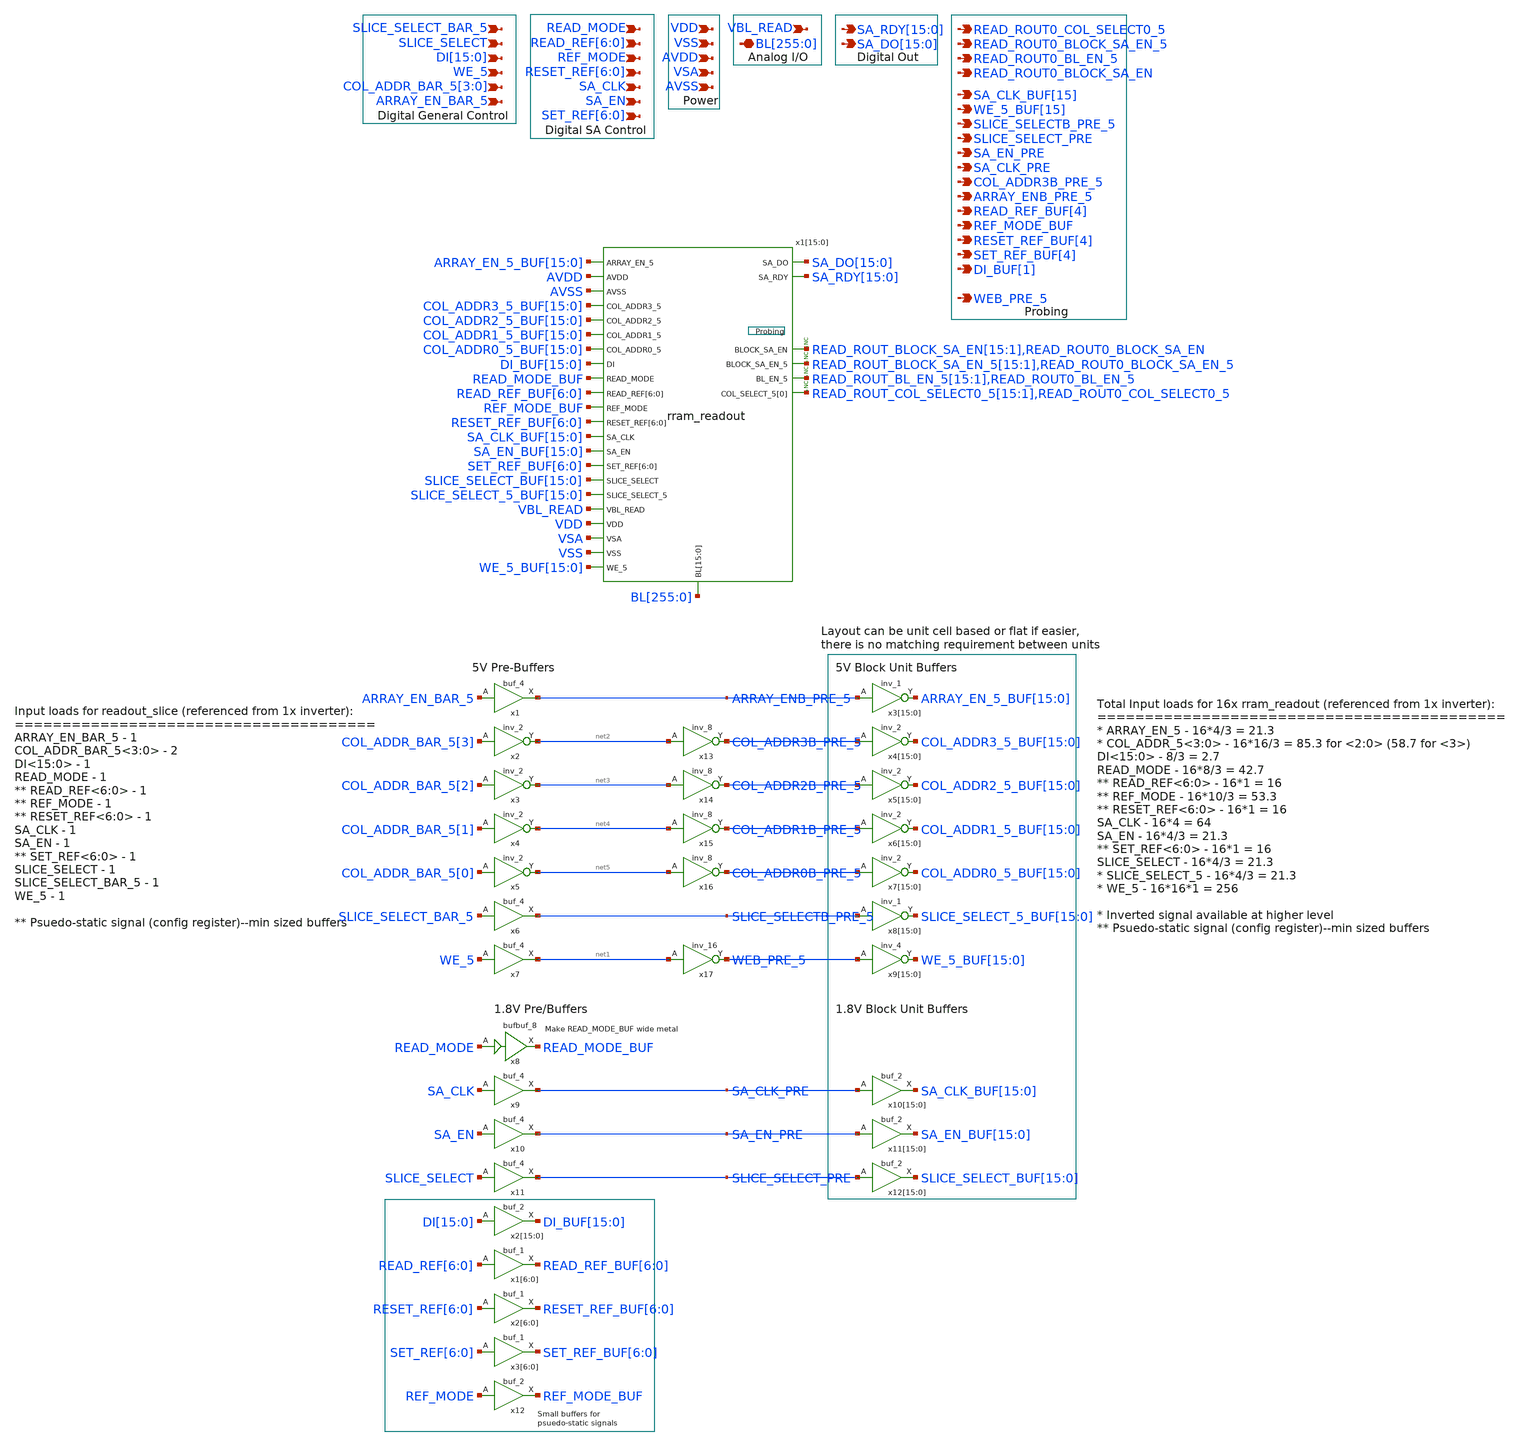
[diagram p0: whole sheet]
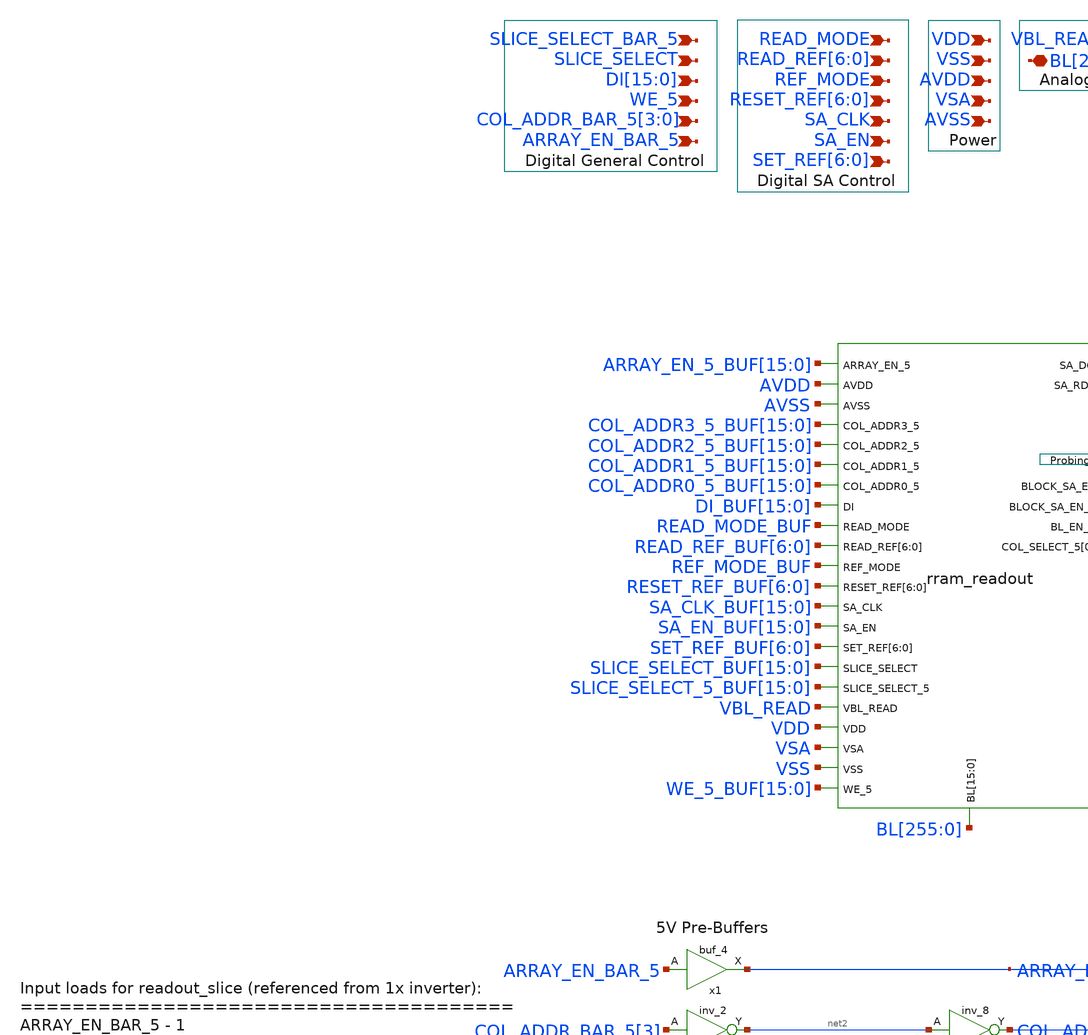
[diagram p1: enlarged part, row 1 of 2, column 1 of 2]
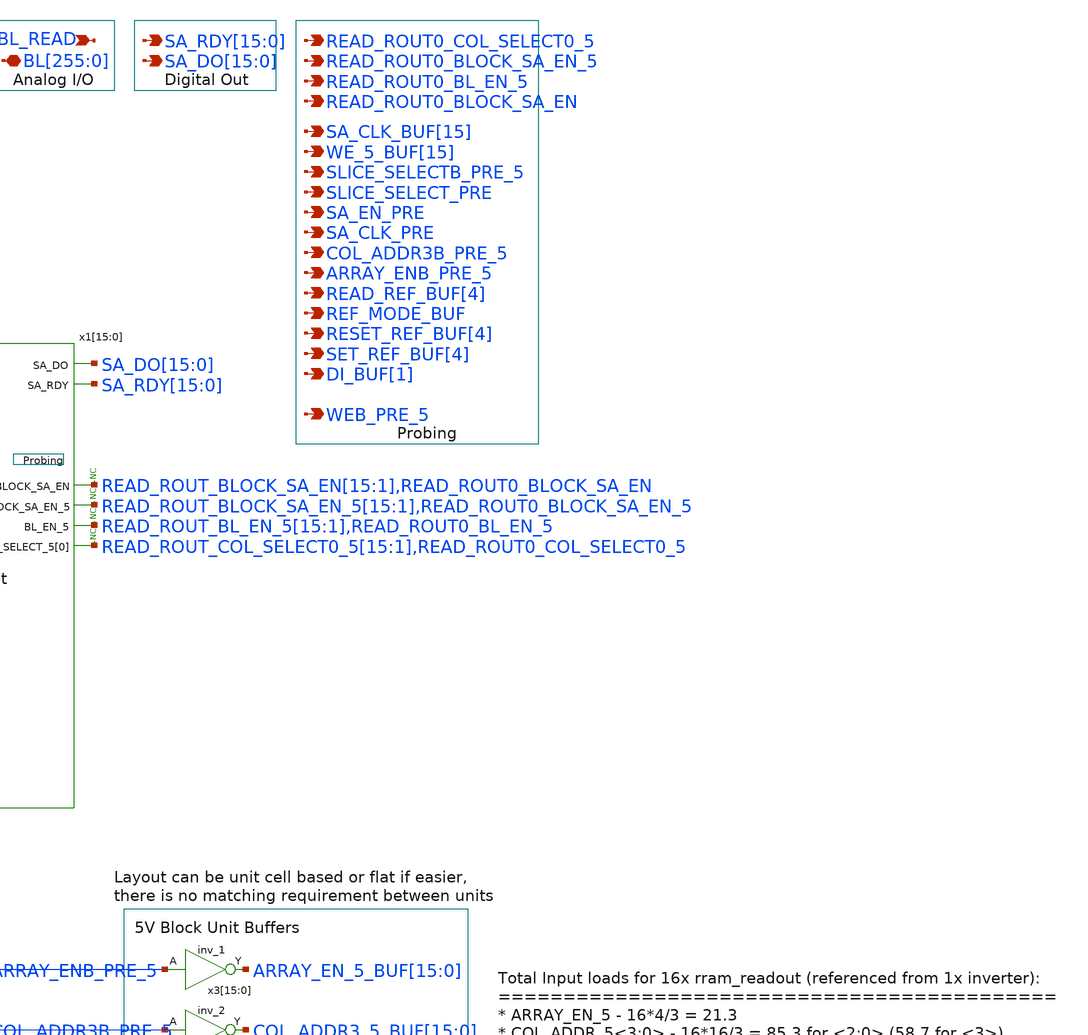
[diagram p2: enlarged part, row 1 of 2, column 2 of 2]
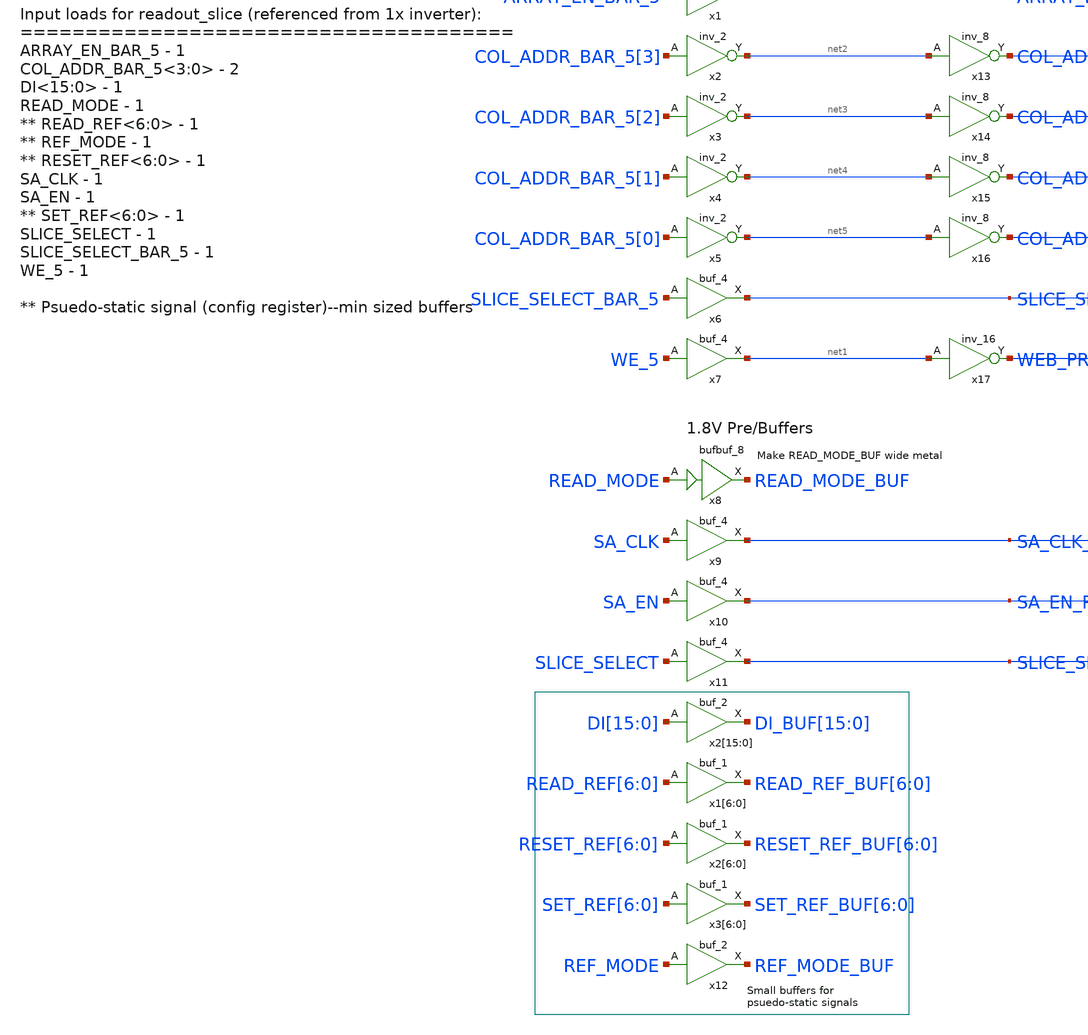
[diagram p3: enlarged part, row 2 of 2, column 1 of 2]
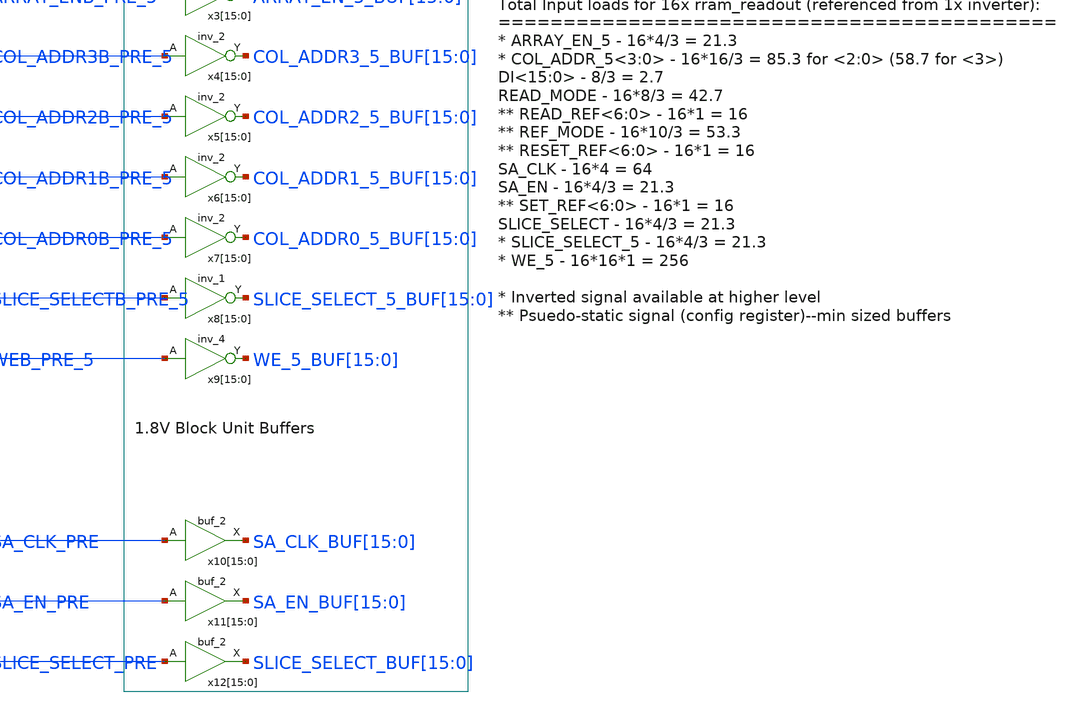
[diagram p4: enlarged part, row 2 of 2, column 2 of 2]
** sch_path: BL_Read_Interface/readout_slice.sch
**.subckt readout_slice SLICE_SELECT_BAR_5 SLICE_SELECT
*+ DI[15],DI[14],DI[13],DI[12],DI[11],DI[10],DI[9],DI[8],DI[7],DI[6],DI[5],DI[4],DI[3],DI[2],DI[1],DI[0] WE_5 COL_ADDR_BAR_5[3],COL_ADDR_BAR_5[2],COL_ADDR_BAR_5[1],COL_ADDR_BAR_5[0] ARRAY_EN_BAR_5 VDD VSS
*+ AVDD VSA AVSS VBL_READ
*+ BL[255],BL[254],BL[253],BL[252],BL[251],BL[250],BL[249],BL[248],BL[247],BL[246],BL[245],BL[244],BL[243],BL[242],BL[241],BL[240],BL[239],BL[238],BL[237],BL[236],BL[235],BL[234],BL[233],BL[232],BL[231],BL[230],BL[229],BL[228],BL[227],BL[226],BL[225],BL[224],BL[223],BL[222],BL[221],BL[220],BL[219],BL[218],BL[217],BL[216],BL[215],BL[214],BL[213],BL[212],BL[211],BL[210],BL[209],BL[208],BL[207],BL[206],BL[205],BL[204],BL[203],BL[202],BL[201],BL[200],BL[199],BL[198],BL[197],BL[196],BL[195],BL[194],BL[193],BL[192],BL[191],BL[190],BL[189],BL[188],BL[187],BL[186],BL[185],BL[184],BL[183],BL[182],BL[181],BL[180],BL[179],BL[178],BL[177],BL[176],BL[175],BL[174],BL[173],BL[172],BL[171],BL[170],BL[169],BL[168],BL[167],BL[166],BL[165],BL[164],BL[163],BL[162],BL[161],BL[160],BL[159],BL[158],BL[157],BL[156],BL[155],BL[154],BL[153],BL[152],BL[151],BL[150],BL[149],BL[148],BL[147],BL[146],BL[145],BL[144],BL[143],BL[142],BL[141],BL[140],BL[139],BL[138],BL[137],BL[136],BL[135],BL[134],BL[133],BL[132],BL[131],BL[130],BL[129],BL[128],BL[127],BL[126],BL[125],BL[124],BL[123],BL[122],BL[121],BL[120],BL[119],BL[118],BL[117],BL[116],BL[115],BL[114],BL[113],BL[112],BL[111],BL[110],BL[109],BL[108],BL[107],BL[106],BL[105],BL[104],BL[103],BL[102],BL[101],BL[100],BL[99],BL[98],BL[97],BL[96],BL[95],BL[94],BL[93],BL[92],BL[91],BL[90],BL[89],BL[88],BL[87],BL[86],BL[85],BL[84],BL[83],BL[82],BL[81],BL[80],BL[79],BL[78],BL[77],BL[76],BL[75],BL[74],BL[73],BL[72],BL[71],BL[70],BL[69],BL[68],BL[67],BL[66],BL[65],BL[64],BL[63],BL[62],BL[61],BL[60],BL[59],BL[58],BL[57],BL[56],BL[55],BL[54],BL[53],BL[52],BL[51],BL[50],BL[49],BL[48],BL[47],BL[46],BL[45],BL[44],BL[43],BL[42],BL[41],BL[40],BL[39],BL[38],BL[37],BL[36],BL[35],BL[34],BL[33],BL[32],BL[31],BL[30],BL[29],BL[28],BL[27],BL[26],BL[25],BL[24],BL[23],BL[22],BL[21],BL[20],BL[19],BL[18],BL[17],BL[16],BL[15],BL[14],BL[13],BL[12],BL[11],BL[10],BL[9],BL[8],BL[7],BL[6],BL[5],BL[4],BL[3],BL[2],BL[1],BL[0]
*+ SA_RDY[15],SA_RDY[14],SA_RDY[13],SA_RDY[12],SA_RDY[11],SA_RDY[10],SA_RDY[9],SA_RDY[8],SA_RDY[7],SA_RDY[6],SA_RDY[5],SA_RDY[4],SA_RDY[3],SA_RDY[2],SA_RDY[1],SA_RDY[0]
*+ SA_DO[15],SA_DO[14],SA_DO[13],SA_DO[12],SA_DO[11],SA_DO[10],SA_DO[9],SA_DO[8],SA_DO[7],SA_DO[6],SA_DO[5],SA_DO[4],SA_DO[3],SA_DO[2],SA_DO[1],SA_DO[0] READ_MODE READ_REF[6],READ_REF[5],READ_REF[4],READ_REF[3],READ_REF[2],READ_REF[1],READ_REF[0]
*+ REF_MODE RESET_REF[6],RESET_REF[5],RESET_REF[4],RESET_REF[3],RESET_REF[2],RESET_REF[1],RESET_REF[0] SA_CLK
*+ SA_EN SET_REF[6],SET_REF[5],SET_REF[4],SET_REF[3],SET_REF[2],SET_REF[1],SET_REF[0]
*+ READ_ROUT0_COL_SELECT0_5 READ_ROUT0_BLOCK_SA_EN_5 READ_ROUT0_BL_EN_5 READ_ROUT0_BLOCK_SA_EN SA_CLK_BUF[15] WE_5_BUF[15]
*+ SLICE_SELECTB_PRE_5 SLICE_SELECT_PRE SA_EN_PRE SA_CLK_PRE COL_ADDR3B_PRE_5 ARRAY_ENB_PRE_5 READ_REF_BUF[4] REF_MODE_BUF
*+ RESET_REF_BUF[4] SET_REF_BUF[4] DI_BUF[1] WEB_PRE_5
*.ipin SLICE_SELECT_BAR_5
*.ipin SLICE_SELECT
*.ipin
*+ DI[15],DI[14],DI[13],DI[12],DI[11],DI[10],DI[9],DI[8],DI[7],DI[6],DI[5],DI[4],DI[3],DI[2],DI[1],DI[0]
*.ipin WE_5
*.ipin COL_ADDR_BAR_5[3],COL_ADDR_BAR_5[2],COL_ADDR_BAR_5[1],COL_ADDR_BAR_5[0]
*.ipin ARRAY_EN_BAR_5
*.ipin VDD
*.ipin VSS
*.ipin AVDD
*.ipin VSA
*.ipin AVSS
*.ipin VBL_READ
*.iopin
*+ BL[255],BL[254],BL[253],BL[252],BL[251],BL[250],BL[249],BL[248],BL[247],BL[246],BL[245],BL[244],BL[243],BL[242],BL[241],BL[240],BL[239],BL[238],BL[237],BL[236],BL[235],BL[234],BL[233],BL[232],BL[231],BL[230],BL[229],BL[228],BL[227],BL[226],BL[225],BL[224],BL[223],BL[222],BL[221],BL[220],BL[219],BL[218],BL[217],BL[216],BL[215],BL[214],BL[213],BL[212],BL[211],BL[210],BL[209],BL[208],BL[207],BL[206],BL[205],BL[204],BL[203],BL[202],BL[201],BL[200],BL[199],BL[198],BL[197],BL[196],BL[195],BL[194],BL[193],BL[192],BL[191],BL[190],BL[189],BL[188],BL[187],BL[186],BL[185],BL[184],BL[183],BL[182],BL[181],BL[180],BL[179],BL[178],BL[177],BL[176],BL[175],BL[174],BL[173],BL[172],BL[171],BL[170],BL[169],BL[168],BL[167],BL[166],BL[165],BL[164],BL[163],BL[162],BL[161],BL[160],BL[159],BL[158],BL[157],BL[156],BL[155],BL[154],BL[153],BL[152],BL[151],BL[150],BL[149],BL[148],BL[147],BL[146],BL[145],BL[144],BL[143],BL[142],BL[141],BL[140],BL[139],BL[138],BL[137],BL[136],BL[135],BL[134],BL[133],BL[132],BL[131],BL[130],BL[129],BL[128],BL[127],BL[126],BL[125],BL[124],BL[123],BL[122],BL[121],BL[120],BL[119],BL[118],BL[117],BL[116],BL[115],BL[114],BL[113],BL[112],BL[111],BL[110],BL[109],BL[108],BL[107],BL[106],BL[105],BL[104],BL[103],BL[102],BL[101],BL[100],BL[99],BL[98],BL[97],BL[96],BL[95],BL[94],BL[93],BL[92],BL[91],BL[90],BL[89],BL[88],BL[87],BL[86],BL[85],BL[84],BL[83],BL[82],BL[81],BL[80],BL[79],BL[78],BL[77],BL[76],BL[75],BL[74],BL[73],BL[72],BL[71],BL[70],BL[69],BL[68],BL[67],BL[66],BL[65],BL[64],BL[63],BL[62],BL[61],BL[60],BL[59],BL[58],BL[57],BL[56],BL[55],BL[54],BL[53],BL[52],BL[51],BL[50],BL[49],BL[48],BL[47],BL[46],BL[45],BL[44],BL[43],BL[42],BL[41],BL[40],BL[39],BL[38],BL[37],BL[36],BL[35],BL[34],BL[33],BL[32],BL[31],BL[30],BL[29],BL[28],BL[27],BL[26],BL[25],BL[24],BL[23],BL[22],BL[21],BL[20],BL[19],BL[18],BL[17],BL[16],BL[15],BL[14],BL[13],BL[12],BL[11],BL[10],BL[9],BL[8],BL[7],BL[6],BL[5],BL[4],BL[3],BL[2],BL[1],BL[0]
*.opin
*+ SA_RDY[15],SA_RDY[14],SA_RDY[13],SA_RDY[12],SA_RDY[11],SA_RDY[10],SA_RDY[9],SA_RDY[8],SA_RDY[7],SA_RDY[6],SA_RDY[5],SA_RDY[4],SA_RDY[3],SA_RDY[2],SA_RDY[1],SA_RDY[0]
*.opin
*+ SA_DO[15],SA_DO[14],SA_DO[13],SA_DO[12],SA_DO[11],SA_DO[10],SA_DO[9],SA_DO[8],SA_DO[7],SA_DO[6],SA_DO[5],SA_DO[4],SA_DO[3],SA_DO[2],SA_DO[1],SA_DO[0]
*.ipin READ_MODE
*.ipin READ_REF[6],READ_REF[5],READ_REF[4],READ_REF[3],READ_REF[2],READ_REF[1],READ_REF[0]
*.ipin REF_MODE
*.ipin RESET_REF[6],RESET_REF[5],RESET_REF[4],RESET_REF[3],RESET_REF[2],RESET_REF[1],RESET_REF[0]
*.ipin SA_CLK
*.ipin SA_EN
*.ipin SET_REF[6],SET_REF[5],SET_REF[4],SET_REF[3],SET_REF[2],SET_REF[1],SET_REF[0]
*.opin READ_ROUT0_COL_SELECT0_5
*.opin READ_ROUT0_BLOCK_SA_EN_5
*.opin READ_ROUT0_BL_EN_5
*.opin READ_ROUT0_BLOCK_SA_EN
*.opin SA_CLK_BUF[15]
*.opin WE_5_BUF[15]
*.opin SLICE_SELECTB_PRE_5
*.opin SLICE_SELECT_PRE
*.opin SA_EN_PRE
*.opin SA_CLK_PRE
*.opin COL_ADDR3B_PRE_5
*.opin ARRAY_ENB_PRE_5
*.opin READ_REF_BUF[4]
*.opin REF_MODE_BUF
*.opin RESET_REF_BUF[4]
*.opin SET_REF_BUF[4]
*.opin DI_BUF[1]
*.opin WEB_PRE_5
x1[15] VDD SLICE_SELECT_BUF[15] READ_ROUT_COL_SELECT0_5[15] VBL_READ READ_MODE_BUF BL[255] BL[254]
+ BL[253] BL[252] BL[251] BL[250] BL[249] BL[248] BL[247] BL[246] BL[245] BL[244] BL[243] BL[242] BL[241]
+ BL[240] READ_ROUT_BLOCK_SA_EN[15] DI_BUF[15] READ_REF_BUF[6] READ_REF_BUF[5] READ_REF_BUF[4]
+ READ_REF_BUF[3] READ_REF_BUF[2] READ_REF_BUF[1] READ_REF_BUF[0] VSS READ_ROUT_BLOCK_SA_EN_5[15] AVDD REF_MODE_BUF
+ SLICE_SELECT_5_BUF[15] READ_ROUT_BL_EN_5[15] WE_5_BUF[15] VSA RESET_REF_BUF[6] RESET_REF_BUF[5] RESET_REF_BUF[4]
+ RESET_REF_BUF[3] RESET_REF_BUF[2] RESET_REF_BUF[1] RESET_REF_BUF[0] AVSS COL_ADDR3_5_BUF[15] SET_REF_BUF[6]
+ SET_REF_BUF[5] SET_REF_BUF[4] SET_REF_BUF[3] SET_REF_BUF[2] SET_REF_BUF[1] SET_REF_BUF[0] COL_ADDR2_5_BUF[15]
+ SA_EN_BUF[15] COL_ADDR1_5_BUF[15] SA_CLK_BUF[15] SA_DO[15] COL_ADDR0_5_BUF[15] SA_RDY[15] ARRAY_EN_5_BUF[15]
+ rram_readout
x1[14] VDD SLICE_SELECT_BUF[14] READ_ROUT_COL_SELECT0_5[14] VBL_READ READ_MODE_BUF BL[239] BL[238]
+ BL[237] BL[236] BL[235] BL[234] BL[233] BL[232] BL[231] BL[230] BL[229] BL[228] BL[227] BL[226] BL[225]
+ BL[224] READ_ROUT_BLOCK_SA_EN[14] DI_BUF[14] READ_REF_BUF[6] READ_REF_BUF[5] READ_REF_BUF[4]
+ READ_REF_BUF[3] READ_REF_BUF[2] READ_REF_BUF[1] READ_REF_BUF[0] VSS READ_ROUT_BLOCK_SA_EN_5[14] AVDD REF_MODE_BUF
+ SLICE_SELECT_5_BUF[14] READ_ROUT_BL_EN_5[14] WE_5_BUF[14] VSA RESET_REF_BUF[6] RESET_REF_BUF[5] RESET_REF_BUF[4]
+ RESET_REF_BUF[3] RESET_REF_BUF[2] RESET_REF_BUF[1] RESET_REF_BUF[0] AVSS COL_ADDR3_5_BUF[14] SET_REF_BUF[6]
+ SET_REF_BUF[5] SET_REF_BUF[4] SET_REF_BUF[3] SET_REF_BUF[2] SET_REF_BUF[1] SET_REF_BUF[0] COL_ADDR2_5_BUF[14]
+ SA_EN_BUF[14] COL_ADDR1_5_BUF[14] SA_CLK_BUF[14] SA_DO[14] COL_ADDR0_5_BUF[14] SA_RDY[14] ARRAY_EN_5_BUF[14]
+ rram_readout
x1[13] VDD SLICE_SELECT_BUF[13] READ_ROUT_COL_SELECT0_5[13] VBL_READ READ_MODE_BUF BL[223] BL[222]
+ BL[221] BL[220] BL[219] BL[218] BL[217] BL[216] BL[215] BL[214] BL[213] BL[212] BL[211] BL[210] BL[209]
+ BL[208] READ_ROUT_BLOCK_SA_EN[13] DI_BUF[13] READ_REF_BUF[6] READ_REF_BUF[5] READ_REF_BUF[4]
+ READ_REF_BUF[3] READ_REF_BUF[2] READ_REF_BUF[1] READ_REF_BUF[0] VSS READ_ROUT_BLOCK_SA_EN_5[13] AVDD REF_MODE_BUF
+ SLICE_SELECT_5_BUF[13] READ_ROUT_BL_EN_5[13] WE_5_BUF[13] VSA RESET_REF_BUF[6] RESET_REF_BUF[5] RESET_REF_BUF[4]
+ RESET_REF_BUF[3] RESET_REF_BUF[2] RESET_REF_BUF[1] RESET_REF_BUF[0] AVSS COL_ADDR3_5_BUF[13] SET_REF_BUF[6]
+ SET_REF_BUF[5] SET_REF_BUF[4] SET_REF_BUF[3] SET_REF_BUF[2] SET_REF_BUF[1] SET_REF_BUF[0] COL_ADDR2_5_BUF[13]
+ SA_EN_BUF[13] COL_ADDR1_5_BUF[13] SA_CLK_BUF[13] SA_DO[13] COL_ADDR0_5_BUF[13] SA_RDY[13] ARRAY_EN_5_BUF[13]
+ rram_readout
x1[12] VDD SLICE_SELECT_BUF[12] READ_ROUT_COL_SELECT0_5[12] VBL_READ READ_MODE_BUF BL[207] BL[206]
+ BL[205] BL[204] BL[203] BL[202] BL[201] BL[200] BL[199] BL[198] BL[197] BL[196] BL[195] BL[194] BL[193]
+ BL[192] READ_ROUT_BLOCK_SA_EN[12] DI_BUF[12] READ_REF_BUF[6] READ_REF_BUF[5] READ_REF_BUF[4]
+ READ_REF_BUF[3] READ_REF_BUF[2] READ_REF_BUF[1] READ_REF_BUF[0] VSS READ_ROUT_BLOCK_SA_EN_5[12] AVDD REF_MODE_BUF
+ SLICE_SELECT_5_BUF[12] READ_ROUT_BL_EN_5[12] WE_5_BUF[12] VSA RESET_REF_BUF[6] RESET_REF_BUF[5] RESET_REF_BUF[4]
+ RESET_REF_BUF[3] RESET_REF_BUF[2] RESET_REF_BUF[1] RESET_REF_BUF[0] AVSS COL_ADDR3_5_BUF[12] SET_REF_BUF[6]
+ SET_REF_BUF[5] SET_REF_BUF[4] SET_REF_BUF[3] SET_REF_BUF[2] SET_REF_BUF[1] SET_REF_BUF[0] COL_ADDR2_5_BUF[12]
+ SA_EN_BUF[12] COL_ADDR1_5_BUF[12] SA_CLK_BUF[12] SA_DO[12] COL_ADDR0_5_BUF[12] SA_RDY[12] ARRAY_EN_5_BUF[12]
+ rram_readout
x1[11] VDD SLICE_SELECT_BUF[11] READ_ROUT_COL_SELECT0_5[11] VBL_READ READ_MODE_BUF BL[191] BL[190]
+ BL[189] BL[188] BL[187] BL[186] BL[185] BL[184] BL[183] BL[182] BL[181] BL[180] BL[179] BL[178] BL[177]
+ BL[176] READ_ROUT_BLOCK_SA_EN[11] DI_BUF[11] READ_REF_BUF[6] READ_REF_BUF[5] READ_REF_BUF[4]
+ READ_REF_BUF[3] READ_REF_BUF[2] READ_REF_BUF[1] READ_REF_BUF[0] VSS READ_ROUT_BLOCK_SA_EN_5[11] AVDD REF_MODE_BUF
+ SLICE_SELECT_5_BUF[11] READ_ROUT_BL_EN_5[11] WE_5_BUF[11] VSA RESET_REF_BUF[6] RESET_REF_BUF[5] RESET_REF_BUF[4]
+ RESET_REF_BUF[3] RESET_REF_BUF[2] RESET_REF_BUF[1] RESET_REF_BUF[0] AVSS COL_ADDR3_5_BUF[11] SET_REF_BUF[6]
+ SET_REF_BUF[5] SET_REF_BUF[4] SET_REF_BUF[3] SET_REF_BUF[2] SET_REF_BUF[1] SET_REF_BUF[0] COL_ADDR2_5_BUF[11]
+ SA_EN_BUF[11] COL_ADDR1_5_BUF[11] SA_CLK_BUF[11] SA_DO[11] COL_ADDR0_5_BUF[11] SA_RDY[11] ARRAY_EN_5_BUF[11]
+ rram_readout
x1[10] VDD SLICE_SELECT_BUF[10] READ_ROUT_COL_SELECT0_5[10] VBL_READ READ_MODE_BUF BL[175] BL[174]
+ BL[173] BL[172] BL[171] BL[170] BL[169] BL[168] BL[167] BL[166] BL[165] BL[164] BL[163] BL[162] BL[161]
+ BL[160] READ_ROUT_BLOCK_SA_EN[10] DI_BUF[10] READ_REF_BUF[6] READ_REF_BUF[5] READ_REF_BUF[4]
+ READ_REF_BUF[3] READ_REF_BUF[2] READ_REF_BUF[1] READ_REF_BUF[0] VSS READ_ROUT_BLOCK_SA_EN_5[10] AVDD REF_MODE_BUF
+ SLICE_SELECT_5_BUF[10] READ_ROUT_BL_EN_5[10] WE_5_BUF[10] VSA RESET_REF_BUF[6] RESET_REF_BUF[5] RESET_REF_BUF[4]
+ RESET_REF_BUF[3] RESET_REF_BUF[2] RESET_REF_BUF[1] RESET_REF_BUF[0] AVSS COL_ADDR3_5_BUF[10] SET_REF_BUF[6]
+ SET_REF_BUF[5] SET_REF_BUF[4] SET_REF_BUF[3] SET_REF_BUF[2] SET_REF_BUF[1] SET_REF_BUF[0] COL_ADDR2_5_BUF[10]
+ SA_EN_BUF[10] COL_ADDR1_5_BUF[10] SA_CLK_BUF[10] SA_DO[10] COL_ADDR0_5_BUF[10] SA_RDY[10] ARRAY_EN_5_BUF[10]
+ rram_readout
x1[9] VDD SLICE_SELECT_BUF[9] READ_ROUT_COL_SELECT0_5[9] VBL_READ READ_MODE_BUF BL[159] BL[158]
+ BL[157] BL[156] BL[155] BL[154] BL[153] BL[152] BL[151] BL[150] BL[149] BL[148] BL[147] BL[146] BL[145]
+ BL[144] READ_ROUT_BLOCK_SA_EN[9] DI_BUF[9] READ_REF_BUF[6] READ_REF_BUF[5] READ_REF_BUF[4] READ_REF_BUF[3]
+ READ_REF_BUF[2] READ_REF_BUF[1] READ_REF_BUF[0] VSS READ_ROUT_BLOCK_SA_EN_5[9] AVDD REF_MODE_BUF
+ SLICE_SELECT_5_BUF[9] READ_ROUT_BL_EN_5[9] WE_5_BUF[9] VSA RESET_REF_BUF[6] RESET_REF_BUF[5] RESET_REF_BUF[4]
+ RESET_REF_BUF[3] RESET_REF_BUF[2] RESET_REF_BUF[1] RESET_REF_BUF[0] AVSS COL_ADDR3_5_BUF[9] SET_REF_BUF[6]
+ SET_REF_BUF[5] SET_REF_BUF[4] SET_REF_BUF[3] SET_REF_BUF[2] SET_REF_BUF[1] SET_REF_BUF[0] COL_ADDR2_5_BUF[9]
+ SA_EN_BUF[9] COL_ADDR1_5_BUF[9] SA_CLK_BUF[9] SA_DO[9] COL_ADDR0_5_BUF[9] SA_RDY[9] ARRAY_EN_5_BUF[9]
+ rram_readout
x1[8] VDD SLICE_SELECT_BUF[8] READ_ROUT_COL_SELECT0_5[8] VBL_READ READ_MODE_BUF BL[143] BL[142]
+ BL[141] BL[140] BL[139] BL[138] BL[137] BL[136] BL[135] BL[134] BL[133] BL[132] BL[131] BL[130] BL[129]
+ BL[128] READ_ROUT_BLOCK_SA_EN[8] DI_BUF[8] READ_REF_BUF[6] READ_REF_BUF[5] READ_REF_BUF[4] READ_REF_BUF[3]
+ READ_REF_BUF[2] READ_REF_BUF[1] READ_REF_BUF[0] VSS READ_ROUT_BLOCK_SA_EN_5[8] AVDD REF_MODE_BUF
+ SLICE_SELECT_5_BUF[8] READ_ROUT_BL_EN_5[8] WE_5_BUF[8] VSA RESET_REF_BUF[6] RESET_REF_BUF[5] RESET_REF_BUF[4]
+ RESET_REF_BUF[3] RESET_REF_BUF[2] RESET_REF_BUF[1] RESET_REF_BUF[0] AVSS COL_ADDR3_5_BUF[8] SET_REF_BUF[6]
+ SET_REF_BUF[5] SET_REF_BUF[4] SET_REF_BUF[3] SET_REF_BUF[2] SET_REF_BUF[1] SET_REF_BUF[0] COL_ADDR2_5_BUF[8]
+ SA_EN_BUF[8] COL_ADDR1_5_BUF[8] SA_CLK_BUF[8] SA_DO[8] COL_ADDR0_5_BUF[8] SA_RDY[8] ARRAY_EN_5_BUF[8]
+ rram_readout
x1[7] VDD SLICE_SELECT_BUF[7] READ_ROUT_COL_SELECT0_5[7] VBL_READ READ_MODE_BUF BL[127] BL[126]
+ BL[125] BL[124] BL[123] BL[122] BL[121] BL[120] BL[119] BL[118] BL[117] BL[116] BL[115] BL[114] BL[113]
+ BL[112] READ_ROUT_BLOCK_SA_EN[7] DI_BUF[7] READ_REF_BUF[6] READ_REF_BUF[5] READ_REF_BUF[4] READ_REF_BUF[3]
+ READ_REF_BUF[2] READ_REF_BUF[1] READ_REF_BUF[0] VSS READ_ROUT_BLOCK_SA_EN_5[7] AVDD REF_MODE_BUF
+ SLICE_SELECT_5_BUF[7] READ_ROUT_BL_EN_5[7] WE_5_BUF[7] VSA RESET_REF_BUF[6] RESET_REF_BUF[5] RESET_REF_BUF[4]
+ RESET_REF_BUF[3] RESET_REF_BUF[2] RESET_REF_BUF[1] RESET_REF_BUF[0] AVSS COL_ADDR3_5_BUF[7] SET_REF_BUF[6]
+ SET_REF_BUF[5] SET_REF_BUF[4] SET_REF_BUF[3] SET_REF_BUF[2] SET_REF_BUF[1] SET_REF_BUF[0] COL_ADDR2_5_BUF[7]
+ SA_EN_BUF[7] COL_ADDR1_5_BUF[7] SA_CLK_BUF[7] SA_DO[7] COL_ADDR0_5_BUF[7] SA_RDY[7] ARRAY_EN_5_BUF[7]
+ rram_readout
x1[6] VDD SLICE_SELECT_BUF[6] READ_ROUT_COL_SELECT0_5[6] VBL_READ READ_MODE_BUF BL[111] BL[110]
+ BL[109] BL[108] BL[107] BL[106] BL[105] BL[104] BL[103] BL[102] BL[101] BL[100] BL[99] BL[98] BL[97] BL[96]
+ READ_ROUT_BLOCK_SA_EN[6] DI_BUF[6] READ_REF_BUF[6] READ_REF_BUF[5] READ_REF_BUF[4] READ_REF_BUF[3] READ_REF_BUF[2]
+ READ_REF_BUF[1] READ_REF_BUF[0] VSS READ_ROUT_BLOCK_SA_EN_5[6] AVDD REF_MODE_BUF SLICE_SELECT_5_BUF[6]
+ READ_ROUT_BL_EN_5[6] WE_5_BUF[6] VSA RESET_REF_BUF[6] RESET_REF_BUF[5] RESET_REF_BUF[4] RESET_REF_BUF[3]
+ RESET_REF_BUF[2] RESET_REF_BUF[1] RESET_REF_BUF[0] AVSS COL_ADDR3_5_BUF[6] SET_REF_BUF[6] SET_REF_BUF[5]
+ SET_REF_BUF[4] SET_REF_BUF[3] SET_REF_BUF[2] SET_REF_BUF[1] SET_REF_BUF[0] COL_ADDR2_5_BUF[6] SA_EN_BUF[6]
+ COL_ADDR1_5_BUF[6] SA_CLK_BUF[6] SA_DO[6] COL_ADDR0_5_BUF[6] SA_RDY[6] ARRAY_EN_5_BUF[6] rram_readout
x1[5] VDD SLICE_SELECT_BUF[5] READ_ROUT_COL_SELECT0_5[5] VBL_READ READ_MODE_BUF BL[95] BL[94] BL[93]
+ BL[92] BL[91] BL[90] BL[89] BL[88] BL[87] BL[86] BL[85] BL[84] BL[83] BL[82] BL[81] BL[80]
+ READ_ROUT_BLOCK_SA_EN[5] DI_BUF[5] READ_REF_BUF[6] READ_REF_BUF[5] READ_REF_BUF[4] READ_REF_BUF[3] READ_REF_BUF[2]
+ READ_REF_BUF[1] READ_REF_BUF[0] VSS READ_ROUT_BLOCK_SA_EN_5[5] AVDD REF_MODE_BUF SLICE_SELECT_5_BUF[5]
+ READ_ROUT_BL_EN_5[5] WE_5_BUF[5] VSA RESET_REF_BUF[6] RESET_REF_BUF[5] RESET_REF_BUF[4] RESET_REF_BUF[3]
+ RESET_REF_BUF[2] RESET_REF_BUF[1] RESET_REF_BUF[0] AVSS COL_ADDR3_5_BUF[5] SET_REF_BUF[6] SET_REF_BUF[5]
+ SET_REF_BUF[4] SET_REF_BUF[3] SET_REF_BUF[2] SET_REF_BUF[1] SET_REF_BUF[0] COL_ADDR2_5_BUF[5] SA_EN_BUF[5]
+ COL_ADDR1_5_BUF[5] SA_CLK_BUF[5] SA_DO[5] COL_ADDR0_5_BUF[5] SA_RDY[5] ARRAY_EN_5_BUF[5] rram_readout
x1[4] VDD SLICE_SELECT_BUF[4] READ_ROUT_COL_SELECT0_5[4] VBL_READ READ_MODE_BUF BL[79] BL[78] BL[77]
+ BL[76] BL[75] BL[74] BL[73] BL[72] BL[71] BL[70] BL[69] BL[68] BL[67] BL[66] BL[65] BL[64]
+ READ_ROUT_BLOCK_SA_EN[4] DI_BUF[4] READ_REF_BUF[6] READ_REF_BUF[5] READ_REF_BUF[4] READ_REF_BUF[3] READ_REF_BUF[2]
+ READ_REF_BUF[1] READ_REF_BUF[0] VSS READ_ROUT_BLOCK_SA_EN_5[4] AVDD REF_MODE_BUF SLICE_SELECT_5_BUF[4]
+ READ_ROUT_BL_EN_5[4] WE_5_BUF[4] VSA RESET_REF_BUF[6] RESET_REF_BUF[5] RESET_REF_BUF[4] RESET_REF_BUF[3]
+ RESET_REF_BUF[2] RESET_REF_BUF[1] RESET_REF_BUF[0] AVSS COL_ADDR3_5_BUF[4] SET_REF_BUF[6] SET_REF_BUF[5]
+ SET_REF_BUF[4] SET_REF_BUF[3] SET_REF_BUF[2] SET_REF_BUF[1] SET_REF_BUF[0] COL_ADDR2_5_BUF[4] SA_EN_BUF[4]
+ COL_ADDR1_5_BUF[4] SA_CLK_BUF[4] SA_DO[4] COL_ADDR0_5_BUF[4] SA_RDY[4] ARRAY_EN_5_BUF[4] rram_readout
x1[3] VDD SLICE_SELECT_BUF[3] READ_ROUT_COL_SELECT0_5[3] VBL_READ READ_MODE_BUF BL[63] BL[62] BL[61]
+ BL[60] BL[59] BL[58] BL[57] BL[56] BL[55] BL[54] BL[53] BL[52] BL[51] BL[50] BL[49] BL[48]
+ READ_ROUT_BLOCK_SA_EN[3] DI_BUF[3] READ_REF_BUF[6] READ_REF_BUF[5] READ_REF_BUF[4] READ_REF_BUF[3] READ_REF_BUF[2]
+ READ_REF_BUF[1] READ_REF_BUF[0] VSS READ_ROUT_BLOCK_SA_EN_5[3] AVDD REF_MODE_BUF SLICE_SELECT_5_BUF[3]
+ READ_ROUT_BL_EN_5[3] WE_5_BUF[3] VSA RESET_REF_BUF[6] RESET_REF_BUF[5] RESET_REF_BUF[4] RESET_REF_BUF[3]
+ RESET_REF_BUF[2] RESET_REF_BUF[1] RESET_REF_BUF[0] AVSS COL_ADDR3_5_BUF[3] SET_REF_BUF[6] SET_REF_BUF[5]
+ SET_REF_BUF[4] SET_REF_BUF[3] SET_REF_BUF[2] SET_REF_BUF[1] SET_REF_BUF[0] COL_ADDR2_5_BUF[3] SA_EN_BUF[3]
+ COL_ADDR1_5_BUF[3] SA_CLK_BUF[3] SA_DO[3] COL_ADDR0_5_BUF[3] SA_RDY[3] ARRAY_EN_5_BUF[3] rram_readout
x1[2] VDD SLICE_SELECT_BUF[2] READ_ROUT_COL_SELECT0_5[2] VBL_READ READ_MODE_BUF BL[47] BL[46] BL[45]
+ BL[44] BL[43] BL[42] BL[41] BL[40] BL[39] BL[38] BL[37] BL[36] BL[35] BL[34] BL[33] BL[32]
+ READ_ROUT_BLOCK_SA_EN[2] DI_BUF[2] READ_REF_BUF[6] READ_REF_BUF[5] READ_REF_BUF[4] READ_REF_BUF[3] READ_REF_BUF[2]
+ READ_REF_BUF[1] READ_REF_BUF[0] VSS READ_ROUT_BLOCK_SA_EN_5[2] AVDD REF_MODE_BUF SLICE_SELECT_5_BUF[2]
+ READ_ROUT_BL_EN_5[2] WE_5_BUF[2] VSA RESET_REF_BUF[6] RESET_REF_BUF[5] RESET_REF_BUF[4] RESET_REF_BUF[3]
+ RESET_REF_BUF[2] RESET_REF_BUF[1] RESET_REF_BUF[0] AVSS COL_ADDR3_5_BUF[2] SET_REF_BUF[6] SET_REF_BUF[5]
+ SET_REF_BUF[4] SET_REF_BUF[3] SET_REF_BUF[2] SET_REF_BUF[1] SET_REF_BUF[0] COL_ADDR2_5_BUF[2] SA_EN_BUF[2]
+ COL_ADDR1_5_BUF[2] SA_CLK_BUF[2] SA_DO[2] COL_ADDR0_5_BUF[2] SA_RDY[2] ARRAY_EN_5_BUF[2] rram_readout
x1[1] VDD SLICE_SELECT_BUF[1] READ_ROUT_COL_SELECT0_5[1] VBL_READ READ_MODE_BUF BL[31] BL[30] BL[29]
+ BL[28] BL[27] BL[26] BL[25] BL[24] BL[23] BL[22] BL[21] BL[20] BL[19] BL[18] BL[17] BL[16]
+ READ_ROUT_BLOCK_SA_EN[1] DI_BUF[1] READ_REF_BUF[6] READ_REF_BUF[5] READ_REF_BUF[4] READ_REF_BUF[3] READ_REF_BUF[2]
+ READ_REF_BUF[1] READ_REF_BUF[0] VSS READ_ROUT_BLOCK_SA_EN_5[1] AVDD REF_MODE_BUF SLICE_SELECT_5_BUF[1]
+ READ_ROUT_BL_EN_5[1] WE_5_BUF[1] VSA RESET_REF_BUF[6] RESET_REF_BUF[5] RESET_REF_BUF[4] RESET_REF_BUF[3]
+ RESET_REF_BUF[2] RESET_REF_BUF[1] RESET_REF_BUF[0] AVSS COL_ADDR3_5_BUF[1] SET_REF_BUF[6] SET_REF_BUF[5]
+ SET_REF_BUF[4] SET_REF_BUF[3] SET_REF_BUF[2] SET_REF_BUF[1] SET_REF_BUF[0] COL_ADDR2_5_BUF[1] SA_EN_BUF[1]
+ COL_ADDR1_5_BUF[1] SA_CLK_BUF[1] SA_DO[1] COL_ADDR0_5_BUF[1] SA_RDY[1] ARRAY_EN_5_BUF[1] rram_readout
x1[0] VDD SLICE_SELECT_BUF[0] READ_ROUT0_COL_SELECT0_5 VBL_READ READ_MODE_BUF BL[15] BL[14] BL[13]
+ BL[12] BL[11] BL[10] BL[9] BL[8] BL[7] BL[6] BL[5] BL[4] BL[3] BL[2] BL[1] BL[0] READ_ROUT0_BLOCK_SA_EN
+ DI_BUF[0] READ_REF_BUF[6] READ_REF_BUF[5] READ_REF_BUF[4] READ_REF_BUF[3] READ_REF_BUF[2] READ_REF_BUF[1]
+ READ_REF_BUF[0] VSS READ_ROUT0_BLOCK_SA_EN_5 AVDD REF_MODE_BUF SLICE_SELECT_5_BUF[0] READ_ROUT0_BL_EN_5 WE_5_BUF[0]
+ VSA RESET_REF_BUF[6] RESET_REF_BUF[5] RESET_REF_BUF[4] RESET_REF_BUF[3] RESET_REF_BUF[2]
+ RESET_REF_BUF[1] RESET_REF_BUF[0] AVSS COL_ADDR3_5_BUF[0] SET_REF_BUF[6] SET_REF_BUF[5] SET_REF_BUF[4]
+ SET_REF_BUF[3] SET_REF_BUF[2] SET_REF_BUF[1] SET_REF_BUF[0] COL_ADDR2_5_BUF[0] SA_EN_BUF[0] COL_ADDR1_5_BUF[0]
+ SA_CLK_BUF[0] SA_DO[0] COL_ADDR0_5_BUF[0] SA_RDY[0] ARRAY_EN_5_BUF[0] rram_readout
x1 ARRAY_EN_BAR_5 VSS VSS AVDD AVDD ARRAY_ENB_PRE_5 sky130_fd_sc_hd__buf_4
x6 SLICE_SELECT_BAR_5 VSS VSS AVDD AVDD SLICE_SELECTB_PRE_5 sky130_fd_sc_hd__buf_4
x7 WE_5 VSS VSS AVDD AVDD net1 sky130_fd_sc_hd__buf_4
x2 COL_ADDR_BAR_5[3] VSS VSS AVDD AVDD net2 sky130_fd_sc_hd__inv_2
x3 COL_ADDR_BAR_5[2] VSS VSS AVDD AVDD net3 sky130_fd_sc_hd__inv_2
x4 COL_ADDR_BAR_5[1] VSS VSS AVDD AVDD net4 sky130_fd_sc_hd__inv_2
x5 COL_ADDR_BAR_5[0] VSS VSS AVDD AVDD net5 sky130_fd_sc_hd__inv_2
x8 READ_MODE VSS VSS VDD VDD READ_MODE_BUF sky130_fd_sc_hd__bufbuf_8
x9 SA_CLK VSS VSS VDD VDD SA_CLK_PRE sky130_fd_sc_hd__buf_4
x10 SA_EN VSS VSS VDD VDD SA_EN_PRE sky130_fd_sc_hd__buf_4
x11 SLICE_SELECT VSS VSS VDD VDD SLICE_SELECT_PRE sky130_fd_sc_hd__buf_4
x2[15] DI[15] VSS VSS VDD VDD DI_BUF[15] sky130_fd_sc_hd__buf_2
x2[14] DI[14] VSS VSS VDD VDD DI_BUF[14] sky130_fd_sc_hd__buf_2
x2[13] DI[13] VSS VSS VDD VDD DI_BUF[13] sky130_fd_sc_hd__buf_2
x2[12] DI[12] VSS VSS VDD VDD DI_BUF[12] sky130_fd_sc_hd__buf_2
x2[11] DI[11] VSS VSS VDD VDD DI_BUF[11] sky130_fd_sc_hd__buf_2
x2[10] DI[10] VSS VSS VDD VDD DI_BUF[10] sky130_fd_sc_hd__buf_2
x2[9] DI[9] VSS VSS VDD VDD DI_BUF[9] sky130_fd_sc_hd__buf_2
x2[8] DI[8] VSS VSS VDD VDD DI_BUF[8] sky130_fd_sc_hd__buf_2
x2[7] DI[7] VSS VSS VDD VDD DI_BUF[7] sky130_fd_sc_hd__buf_2
x2[6] DI[6] VSS VSS VDD VDD DI_BUF[6] sky130_fd_sc_hd__buf_2
x2[5] DI[5] VSS VSS VDD VDD DI_BUF[5] sky130_fd_sc_hd__buf_2
x2[4] DI[4] VSS VSS VDD VDD DI_BUF[4] sky130_fd_sc_hd__buf_2
x2[3] DI[3] VSS VSS VDD VDD DI_BUF[3] sky130_fd_sc_hd__buf_2
x2[2] DI[2] VSS VSS VDD VDD DI_BUF[2] sky130_fd_sc_hd__buf_2
x2[1] DI[1] VSS VSS VDD VDD DI_BUF[1] sky130_fd_sc_hd__buf_2
x2[0] DI[0] VSS VSS VDD VDD DI_BUF[0] sky130_fd_sc_hd__buf_2
x1[6] READ_REF[6] VSS VSS VDD VDD READ_REF_BUF[6] sky130_fd_sc_hd__buf_1
x1[5] READ_REF[5] VSS VSS VDD VDD READ_REF_BUF[5] sky130_fd_sc_hd__buf_1
x1[4] READ_REF[4] VSS VSS VDD VDD READ_REF_BUF[4] sky130_fd_sc_hd__buf_1
x1[3] READ_REF[3] VSS VSS VDD VDD READ_REF_BUF[3] sky130_fd_sc_hd__buf_1
x1[2] READ_REF[2] VSS VSS VDD VDD READ_REF_BUF[2] sky130_fd_sc_hd__buf_1
x1[1] READ_REF[1] VSS VSS VDD VDD READ_REF_BUF[1] sky130_fd_sc_hd__buf_1
x1[0] READ_REF[0] VSS VSS VDD VDD READ_REF_BUF[0] sky130_fd_sc_hd__buf_1
x2[6] RESET_REF[6] VSS VSS VDD VDD RESET_REF_BUF[6] sky130_fd_sc_hd__buf_1
x2[5] RESET_REF[5] VSS VSS VDD VDD RESET_REF_BUF[5] sky130_fd_sc_hd__buf_1
x2[4] RESET_REF[4] VSS VSS VDD VDD RESET_REF_BUF[4] sky130_fd_sc_hd__buf_1
x2[3] RESET_REF[3] VSS VSS VDD VDD RESET_REF_BUF[3] sky130_fd_sc_hd__buf_1
x2[2] RESET_REF[2] VSS VSS VDD VDD RESET_REF_BUF[2] sky130_fd_sc_hd__buf_1
x2[1] RESET_REF[1] VSS VSS VDD VDD RESET_REF_BUF[1] sky130_fd_sc_hd__buf_1
x2[0] RESET_REF[0] VSS VSS VDD VDD RESET_REF_BUF[0] sky130_fd_sc_hd__buf_1
x3[6] SET_REF[6] VSS VSS VDD VDD SET_REF_BUF[6] sky130_fd_sc_hd__buf_1
x3[5] SET_REF[5] VSS VSS VDD VDD SET_REF_BUF[5] sky130_fd_sc_hd__buf_1
x3[4] SET_REF[4] VSS VSS VDD VDD SET_REF_BUF[4] sky130_fd_sc_hd__buf_1
x3[3] SET_REF[3] VSS VSS VDD VDD SET_REF_BUF[3] sky130_fd_sc_hd__buf_1
x3[2] SET_REF[2] VSS VSS VDD VDD SET_REF_BUF[2] sky130_fd_sc_hd__buf_1
x3[1] SET_REF[1] VSS VSS VDD VDD SET_REF_BUF[1] sky130_fd_sc_hd__buf_1
x3[0] SET_REF[0] VSS VSS VDD VDD SET_REF_BUF[0] sky130_fd_sc_hd__buf_1
x12 REF_MODE VSS VSS VDD VDD REF_MODE_BUF sky130_fd_sc_hd__buf_2
x13 net2 VSS VSS AVDD AVDD COL_ADDR3B_PRE_5 sky130_fd_sc_hd__inv_8
x14 net3 VSS VSS AVDD AVDD COL_ADDR2B_PRE_5 sky130_fd_sc_hd__inv_8
x15 net4 VSS VSS AVDD AVDD COL_ADDR1B_PRE_5 sky130_fd_sc_hd__inv_8
x16 net5 VSS VSS AVDD AVDD COL_ADDR0B_PRE_5 sky130_fd_sc_hd__inv_8
x3[15] ARRAY_ENB_PRE_5 VSS VSS AVDD AVDD ARRAY_EN_5_BUF[15] sky130_fd_sc_hd__inv_1
x3[14] ARRAY_ENB_PRE_5 VSS VSS AVDD AVDD ARRAY_EN_5_BUF[14] sky130_fd_sc_hd__inv_1
x3[13] ARRAY_ENB_PRE_5 VSS VSS AVDD AVDD ARRAY_EN_5_BUF[13] sky130_fd_sc_hd__inv_1
x3[12] ARRAY_ENB_PRE_5 VSS VSS AVDD AVDD ARRAY_EN_5_BUF[12] sky130_fd_sc_hd__inv_1
x3[11] ARRAY_ENB_PRE_5 VSS VSS AVDD AVDD ARRAY_EN_5_BUF[11] sky130_fd_sc_hd__inv_1
x3[10] ARRAY_ENB_PRE_5 VSS VSS AVDD AVDD ARRAY_EN_5_BUF[10] sky130_fd_sc_hd__inv_1
x3[9] ARRAY_ENB_PRE_5 VSS VSS AVDD AVDD ARRAY_EN_5_BUF[9] sky130_fd_sc_hd__inv_1
x3[8] ARRAY_ENB_PRE_5 VSS VSS AVDD AVDD ARRAY_EN_5_BUF[8] sky130_fd_sc_hd__inv_1
x3[7] ARRAY_ENB_PRE_5 VSS VSS AVDD AVDD ARRAY_EN_5_BUF[7] sky130_fd_sc_hd__inv_1
x3[6] ARRAY_ENB_PRE_5 VSS VSS AVDD AVDD ARRAY_EN_5_BUF[6] sky130_fd_sc_hd__inv_1
x3[5] ARRAY_ENB_PRE_5 VSS VSS AVDD AVDD ARRAY_EN_5_BUF[5] sky130_fd_sc_hd__inv_1
x3[4] ARRAY_ENB_PRE_5 VSS VSS AVDD AVDD ARRAY_EN_5_BUF[4] sky130_fd_sc_hd__inv_1
x3[3] ARRAY_ENB_PRE_5 VSS VSS AVDD AVDD ARRAY_EN_5_BUF[3] sky130_fd_sc_hd__inv_1
x3[2] ARRAY_ENB_PRE_5 VSS VSS AVDD AVDD ARRAY_EN_5_BUF[2] sky130_fd_sc_hd__inv_1
x3[1] ARRAY_ENB_PRE_5 VSS VSS AVDD AVDD ARRAY_EN_5_BUF[1] sky130_fd_sc_hd__inv_1
x3[0] ARRAY_ENB_PRE_5 VSS VSS AVDD AVDD ARRAY_EN_5_BUF[0] sky130_fd_sc_hd__inv_1
x4[15] COL_ADDR3B_PRE_5 VSS VSS AVDD AVDD COL_ADDR3_5_BUF[15] sky130_fd_sc_hd__inv_2
x4[14] COL_ADDR3B_PRE_5 VSS VSS AVDD AVDD COL_ADDR3_5_BUF[14] sky130_fd_sc_hd__inv_2
x4[13] COL_ADDR3B_PRE_5 VSS VSS AVDD AVDD COL_ADDR3_5_BUF[13] sky130_fd_sc_hd__inv_2
x4[12] COL_ADDR3B_PRE_5 VSS VSS AVDD AVDD COL_ADDR3_5_BUF[12] sky130_fd_sc_hd__inv_2
x4[11] COL_ADDR3B_PRE_5 VSS VSS AVDD AVDD COL_ADDR3_5_BUF[11] sky130_fd_sc_hd__inv_2
x4[10] COL_ADDR3B_PRE_5 VSS VSS AVDD AVDD COL_ADDR3_5_BUF[10] sky130_fd_sc_hd__inv_2
x4[9] COL_ADDR3B_PRE_5 VSS VSS AVDD AVDD COL_ADDR3_5_BUF[9] sky130_fd_sc_hd__inv_2
x4[8] COL_ADDR3B_PRE_5 VSS VSS AVDD AVDD COL_ADDR3_5_BUF[8] sky130_fd_sc_hd__inv_2
x4[7] COL_ADDR3B_PRE_5 VSS VSS AVDD AVDD COL_ADDR3_5_BUF[7] sky130_fd_sc_hd__inv_2
x4[6] COL_ADDR3B_PRE_5 VSS VSS AVDD AVDD COL_ADDR3_5_BUF[6] sky130_fd_sc_hd__inv_2
x4[5] COL_ADDR3B_PRE_5 VSS VSS AVDD AVDD COL_ADDR3_5_BUF[5] sky130_fd_sc_hd__inv_2
x4[4] COL_ADDR3B_PRE_5 VSS VSS AVDD AVDD COL_ADDR3_5_BUF[4] sky130_fd_sc_hd__inv_2
x4[3] COL_ADDR3B_PRE_5 VSS VSS AVDD AVDD COL_ADDR3_5_BUF[3] sky130_fd_sc_hd__inv_2
x4[2] COL_ADDR3B_PRE_5 VSS VSS AVDD AVDD COL_ADDR3_5_BUF[2] sky130_fd_sc_hd__inv_2
x4[1] COL_ADDR3B_PRE_5 VSS VSS AVDD AVDD COL_ADDR3_5_BUF[1] sky130_fd_sc_hd__inv_2
x4[0] COL_ADDR3B_PRE_5 VSS VSS AVDD AVDD COL_ADDR3_5_BUF[0] sky130_fd_sc_hd__inv_2
x5[15] COL_ADDR2B_PRE_5 VSS VSS AVDD AVDD COL_ADDR2_5_BUF[15] sky130_fd_sc_hd__inv_2
x5[14] COL_ADDR2B_PRE_5 VSS VSS AVDD AVDD COL_ADDR2_5_BUF[14] sky130_fd_sc_hd__inv_2
x5[13] COL_ADDR2B_PRE_5 VSS VSS AVDD AVDD COL_ADDR2_5_BUF[13] sky130_fd_sc_hd__inv_2
x5[12] COL_ADDR2B_PRE_5 VSS VSS AVDD AVDD COL_ADDR2_5_BUF[12] sky130_fd_sc_hd__inv_2
x5[11] COL_ADDR2B_PRE_5 VSS VSS AVDD AVDD COL_ADDR2_5_BUF[11] sky130_fd_sc_hd__inv_2
x5[10] COL_ADDR2B_PRE_5 VSS VSS AVDD AVDD COL_ADDR2_5_BUF[10] sky130_fd_sc_hd__inv_2
x5[9] COL_ADDR2B_PRE_5 VSS VSS AVDD AVDD COL_ADDR2_5_BUF[9] sky130_fd_sc_hd__inv_2
x5[8] COL_ADDR2B_PRE_5 VSS VSS AVDD AVDD COL_ADDR2_5_BUF[8] sky130_fd_sc_hd__inv_2
x5[7] COL_ADDR2B_PRE_5 VSS VSS AVDD AVDD COL_ADDR2_5_BUF[7] sky130_fd_sc_hd__inv_2
x5[6] COL_ADDR2B_PRE_5 VSS VSS AVDD AVDD COL_ADDR2_5_BUF[6] sky130_fd_sc_hd__inv_2
x5[5] COL_ADDR2B_PRE_5 VSS VSS AVDD AVDD COL_ADDR2_5_BUF[5] sky130_fd_sc_hd__inv_2
x5[4] COL_ADDR2B_PRE_5 VSS VSS AVDD AVDD COL_ADDR2_5_BUF[4] sky130_fd_sc_hd__inv_2
x5[3] COL_ADDR2B_PRE_5 VSS VSS AVDD AVDD COL_ADDR2_5_BUF[3] sky130_fd_sc_hd__inv_2
x5[2] COL_ADDR2B_PRE_5 VSS VSS AVDD AVDD COL_ADDR2_5_BUF[2] sky130_fd_sc_hd__inv_2
x5[1] COL_ADDR2B_PRE_5 VSS VSS AVDD AVDD COL_ADDR2_5_BUF[1] sky130_fd_sc_hd__inv_2
x5[0] COL_ADDR2B_PRE_5 VSS VSS AVDD AVDD COL_ADDR2_5_BUF[0] sky130_fd_sc_hd__inv_2
x6[15] COL_ADDR1B_PRE_5 VSS VSS AVDD AVDD COL_ADDR1_5_BUF[15] sky130_fd_sc_hd__inv_2
x6[14] COL_ADDR1B_PRE_5 VSS VSS AVDD AVDD COL_ADDR1_5_BUF[14] sky130_fd_sc_hd__inv_2
x6[13] COL_ADDR1B_PRE_5 VSS VSS AVDD AVDD COL_ADDR1_5_BUF[13] sky130_fd_sc_hd__inv_2
x6[12] COL_ADDR1B_PRE_5 VSS VSS AVDD AVDD COL_ADDR1_5_BUF[12] sky130_fd_sc_hd__inv_2
x6[11] COL_ADDR1B_PRE_5 VSS VSS AVDD AVDD COL_ADDR1_5_BUF[11] sky130_fd_sc_hd__inv_2
x6[10] COL_ADDR1B_PRE_5 VSS VSS AVDD AVDD COL_ADDR1_5_BUF[10] sky130_fd_sc_hd__inv_2
x6[9] COL_ADDR1B_PRE_5 VSS VSS AVDD AVDD COL_ADDR1_5_BUF[9] sky130_fd_sc_hd__inv_2
x6[8] COL_ADDR1B_PRE_5 VSS VSS AVDD AVDD COL_ADDR1_5_BUF[8] sky130_fd_sc_hd__inv_2
x6[7] COL_ADDR1B_PRE_5 VSS VSS AVDD AVDD COL_ADDR1_5_BUF[7] sky130_fd_sc_hd__inv_2
x6[6] COL_ADDR1B_PRE_5 VSS VSS AVDD AVDD COL_ADDR1_5_BUF[6] sky130_fd_sc_hd__inv_2
x6[5] COL_ADDR1B_PRE_5 VSS VSS AVDD AVDD COL_ADDR1_5_BUF[5] sky130_fd_sc_hd__inv_2
x6[4] COL_ADDR1B_PRE_5 VSS VSS AVDD AVDD COL_ADDR1_5_BUF[4] sky130_fd_sc_hd__inv_2
x6[3] COL_ADDR1B_PRE_5 VSS VSS AVDD AVDD COL_ADDR1_5_BUF[3] sky130_fd_sc_hd__inv_2
x6[2] COL_ADDR1B_PRE_5 VSS VSS AVDD AVDD COL_ADDR1_5_BUF[2] sky130_fd_sc_hd__inv_2
x6[1] COL_ADDR1B_PRE_5 VSS VSS AVDD AVDD COL_ADDR1_5_BUF[1] sky130_fd_sc_hd__inv_2
x6[0] COL_ADDR1B_PRE_5 VSS VSS AVDD AVDD COL_ADDR1_5_BUF[0] sky130_fd_sc_hd__inv_2
x7[15] COL_ADDR0B_PRE_5 VSS VSS AVDD AVDD COL_ADDR0_5_BUF[15] sky130_fd_sc_hd__inv_2
x7[14] COL_ADDR0B_PRE_5 VSS VSS AVDD AVDD COL_ADDR0_5_BUF[14] sky130_fd_sc_hd__inv_2
x7[13] COL_ADDR0B_PRE_5 VSS VSS AVDD AVDD COL_ADDR0_5_BUF[13] sky130_fd_sc_hd__inv_2
x7[12] COL_ADDR0B_PRE_5 VSS VSS AVDD AVDD COL_ADDR0_5_BUF[12] sky130_fd_sc_hd__inv_2
x7[11] COL_ADDR0B_PRE_5 VSS VSS AVDD AVDD COL_ADDR0_5_BUF[11] sky130_fd_sc_hd__inv_2
x7[10] COL_ADDR0B_PRE_5 VSS VSS AVDD AVDD COL_ADDR0_5_BUF[10] sky130_fd_sc_hd__inv_2
x7[9] COL_ADDR0B_PRE_5 VSS VSS AVDD AVDD COL_ADDR0_5_BUF[9] sky130_fd_sc_hd__inv_2
x7[8] COL_ADDR0B_PRE_5 VSS VSS AVDD AVDD COL_ADDR0_5_BUF[8] sky130_fd_sc_hd__inv_2
x7[7] COL_ADDR0B_PRE_5 VSS VSS AVDD AVDD COL_ADDR0_5_BUF[7] sky130_fd_sc_hd__inv_2
x7[6] COL_ADDR0B_PRE_5 VSS VSS AVDD AVDD COL_ADDR0_5_BUF[6] sky130_fd_sc_hd__inv_2
x7[5] COL_ADDR0B_PRE_5 VSS VSS AVDD AVDD COL_ADDR0_5_BUF[5] sky130_fd_sc_hd__inv_2
x7[4] COL_ADDR0B_PRE_5 VSS VSS AVDD AVDD COL_ADDR0_5_BUF[4] sky130_fd_sc_hd__inv_2
x7[3] COL_ADDR0B_PRE_5 VSS VSS AVDD AVDD COL_ADDR0_5_BUF[3] sky130_fd_sc_hd__inv_2
x7[2] COL_ADDR0B_PRE_5 VSS VSS AVDD AVDD COL_ADDR0_5_BUF[2] sky130_fd_sc_hd__inv_2
x7[1] COL_ADDR0B_PRE_5 VSS VSS AVDD AVDD COL_ADDR0_5_BUF[1] sky130_fd_sc_hd__inv_2
x7[0] COL_ADDR0B_PRE_5 VSS VSS AVDD AVDD COL_ADDR0_5_BUF[0] sky130_fd_sc_hd__inv_2
x8[15] SLICE_SELECTB_PRE_5 VSS VSS AVDD AVDD SLICE_SELECT_5_BUF[15] sky130_fd_sc_hd__inv_1
x8[14] SLICE_SELECTB_PRE_5 VSS VSS AVDD AVDD SLICE_SELECT_5_BUF[14] sky130_fd_sc_hd__inv_1
x8[13] SLICE_SELECTB_PRE_5 VSS VSS AVDD AVDD SLICE_SELECT_5_BUF[13] sky130_fd_sc_hd__inv_1
x8[12] SLICE_SELECTB_PRE_5 VSS VSS AVDD AVDD SLICE_SELECT_5_BUF[12] sky130_fd_sc_hd__inv_1
x8[11] SLICE_SELECTB_PRE_5 VSS VSS AVDD AVDD SLICE_SELECT_5_BUF[11] sky130_fd_sc_hd__inv_1
x8[10] SLICE_SELECTB_PRE_5 VSS VSS AVDD AVDD SLICE_SELECT_5_BUF[10] sky130_fd_sc_hd__inv_1
x8[9] SLICE_SELECTB_PRE_5 VSS VSS AVDD AVDD SLICE_SELECT_5_BUF[9] sky130_fd_sc_hd__inv_1
x8[8] SLICE_SELECTB_PRE_5 VSS VSS AVDD AVDD SLICE_SELECT_5_BUF[8] sky130_fd_sc_hd__inv_1
x8[7] SLICE_SELECTB_PRE_5 VSS VSS AVDD AVDD SLICE_SELECT_5_BUF[7] sky130_fd_sc_hd__inv_1
x8[6] SLICE_SELECTB_PRE_5 VSS VSS AVDD AVDD SLICE_SELECT_5_BUF[6] sky130_fd_sc_hd__inv_1
x8[5] SLICE_SELECTB_PRE_5 VSS VSS AVDD AVDD SLICE_SELECT_5_BUF[5] sky130_fd_sc_hd__inv_1
x8[4] SLICE_SELECTB_PRE_5 VSS VSS AVDD AVDD SLICE_SELECT_5_BUF[4] sky130_fd_sc_hd__inv_1
x8[3] SLICE_SELECTB_PRE_5 VSS VSS AVDD AVDD SLICE_SELECT_5_BUF[3] sky130_fd_sc_hd__inv_1
x8[2] SLICE_SELECTB_PRE_5 VSS VSS AVDD AVDD SLICE_SELECT_5_BUF[2] sky130_fd_sc_hd__inv_1
x8[1] SLICE_SELECTB_PRE_5 VSS VSS AVDD AVDD SLICE_SELECT_5_BUF[1] sky130_fd_sc_hd__inv_1
x8[0] SLICE_SELECTB_PRE_5 VSS VSS AVDD AVDD SLICE_SELECT_5_BUF[0] sky130_fd_sc_hd__inv_1
x17 net1 VSS VSS AVDD AVDD WEB_PRE_5 sky130_fd_sc_hd__inv_16
x9[15] WEB_PRE_5 VSS VSS AVDD AVDD WE_5_BUF[15] sky130_fd_sc_hd__inv_4
x9[14] WEB_PRE_5 VSS VSS AVDD AVDD WE_5_BUF[14] sky130_fd_sc_hd__inv_4
x9[13] WEB_PRE_5 VSS VSS AVDD AVDD WE_5_BUF[13] sky130_fd_sc_hd__inv_4
x9[12] WEB_PRE_5 VSS VSS AVDD AVDD WE_5_BUF[12] sky130_fd_sc_hd__inv_4
x9[11] WEB_PRE_5 VSS VSS AVDD AVDD WE_5_BUF[11] sky130_fd_sc_hd__inv_4
x9[10] WEB_PRE_5 VSS VSS AVDD AVDD WE_5_BUF[10] sky130_fd_sc_hd__inv_4
x9[9] WEB_PRE_5 VSS VSS AVDD AVDD WE_5_BUF[9] sky130_fd_sc_hd__inv_4
x9[8] WEB_PRE_5 VSS VSS AVDD AVDD WE_5_BUF[8] sky130_fd_sc_hd__inv_4
x9[7] WEB_PRE_5 VSS VSS AVDD AVDD WE_5_BUF[7] sky130_fd_sc_hd__inv_4
x9[6] WEB_PRE_5 VSS VSS AVDD AVDD WE_5_BUF[6] sky130_fd_sc_hd__inv_4
x9[5] WEB_PRE_5 VSS VSS AVDD AVDD WE_5_BUF[5] sky130_fd_sc_hd__inv_4
x9[4] WEB_PRE_5 VSS VSS AVDD AVDD WE_5_BUF[4] sky130_fd_sc_hd__inv_4
x9[3] WEB_PRE_5 VSS VSS AVDD AVDD WE_5_BUF[3] sky130_fd_sc_hd__inv_4
x9[2] WEB_PRE_5 VSS VSS AVDD AVDD WE_5_BUF[2] sky130_fd_sc_hd__inv_4
x9[1] WEB_PRE_5 VSS VSS AVDD AVDD WE_5_BUF[1] sky130_fd_sc_hd__inv_4
x9[0] WEB_PRE_5 VSS VSS AVDD AVDD WE_5_BUF[0] sky130_fd_sc_hd__inv_4
x10[15] SA_CLK_PRE VSS VSS VDD VDD SA_CLK_BUF[15] sky130_fd_sc_hd__buf_2
x10[14] SA_CLK_PRE VSS VSS VDD VDD SA_CLK_BUF[14] sky130_fd_sc_hd__buf_2
x10[13] SA_CLK_PRE VSS VSS VDD VDD SA_CLK_BUF[13] sky130_fd_sc_hd__buf_2
x10[12] SA_CLK_PRE VSS VSS VDD VDD SA_CLK_BUF[12] sky130_fd_sc_hd__buf_2
x10[11] SA_CLK_PRE VSS VSS VDD VDD SA_CLK_BUF[11] sky130_fd_sc_hd__buf_2
x10[10] SA_CLK_PRE VSS VSS VDD VDD SA_CLK_BUF[10] sky130_fd_sc_hd__buf_2
x10[9] SA_CLK_PRE VSS VSS VDD VDD SA_CLK_BUF[9] sky130_fd_sc_hd__buf_2
x10[8] SA_CLK_PRE VSS VSS VDD VDD SA_CLK_BUF[8] sky130_fd_sc_hd__buf_2
x10[7] SA_CLK_PRE VSS VSS VDD VDD SA_CLK_BUF[7] sky130_fd_sc_hd__buf_2
x10[6] SA_CLK_PRE VSS VSS VDD VDD SA_CLK_BUF[6] sky130_fd_sc_hd__buf_2
x10[5] SA_CLK_PRE VSS VSS VDD VDD SA_CLK_BUF[5] sky130_fd_sc_hd__buf_2
x10[4] SA_CLK_PRE VSS VSS VDD VDD SA_CLK_BUF[4] sky130_fd_sc_hd__buf_2
x10[3] SA_CLK_PRE VSS VSS VDD VDD SA_CLK_BUF[3] sky130_fd_sc_hd__buf_2
x10[2] SA_CLK_PRE VSS VSS VDD VDD SA_CLK_BUF[2] sky130_fd_sc_hd__buf_2
x10[1] SA_CLK_PRE VSS VSS VDD VDD SA_CLK_BUF[1] sky130_fd_sc_hd__buf_2
x10[0] SA_CLK_PRE VSS VSS VDD VDD SA_CLK_BUF[0] sky130_fd_sc_hd__buf_2
x11[15] SA_EN_PRE VSS VSS VDD VDD SA_EN_BUF[15] sky130_fd_sc_hd__buf_2
x11[14] SA_EN_PRE VSS VSS VDD VDD SA_EN_BUF[14] sky130_fd_sc_hd__buf_2
x11[13] SA_EN_PRE VSS VSS VDD VDD SA_EN_BUF[13] sky130_fd_sc_hd__buf_2
x11[12] SA_EN_PRE VSS VSS VDD VDD SA_EN_BUF[12] sky130_fd_sc_hd__buf_2
x11[11] SA_EN_PRE VSS VSS VDD VDD SA_EN_BUF[11] sky130_fd_sc_hd__buf_2
x11[10] SA_EN_PRE VSS VSS VDD VDD SA_EN_BUF[10] sky130_fd_sc_hd__buf_2
x11[9] SA_EN_PRE VSS VSS VDD VDD SA_EN_BUF[9] sky130_fd_sc_hd__buf_2
x11[8] SA_EN_PRE VSS VSS VDD VDD SA_EN_BUF[8] sky130_fd_sc_hd__buf_2
x11[7] SA_EN_PRE VSS VSS VDD VDD SA_EN_BUF[7] sky130_fd_sc_hd__buf_2
x11[6] SA_EN_PRE VSS VSS VDD VDD SA_EN_BUF[6] sky130_fd_sc_hd__buf_2
x11[5] SA_EN_PRE VSS VSS VDD VDD SA_EN_BUF[5] sky130_fd_sc_hd__buf_2
x11[4] SA_EN_PRE VSS VSS VDD VDD SA_EN_BUF[4] sky130_fd_sc_hd__buf_2
x11[3] SA_EN_PRE VSS VSS VDD VDD SA_EN_BUF[3] sky130_fd_sc_hd__buf_2
x11[2] SA_EN_PRE VSS VSS VDD VDD SA_EN_BUF[2] sky130_fd_sc_hd__buf_2
x11[1] SA_EN_PRE VSS VSS VDD VDD SA_EN_BUF[1] sky130_fd_sc_hd__buf_2
x11[0] SA_EN_PRE VSS VSS VDD VDD SA_EN_BUF[0] sky130_fd_sc_hd__buf_2
x12[15] SLICE_SELECT_PRE VSS VSS VDD VDD SLICE_SELECT_BUF[15] sky130_fd_sc_hd__buf_2
x12[14] SLICE_SELECT_PRE VSS VSS VDD VDD SLICE_SELECT_BUF[14] sky130_fd_sc_hd__buf_2
x12[13] SLICE_SELECT_PRE VSS VSS VDD VDD SLICE_SELECT_BUF[13] sky130_fd_sc_hd__buf_2
x12[12] SLICE_SELECT_PRE VSS VSS VDD VDD SLICE_SELECT_BUF[12] sky130_fd_sc_hd__buf_2
x12[11] SLICE_SELECT_PRE VSS VSS VDD VDD SLICE_SELECT_BUF[11] sky130_fd_sc_hd__buf_2
x12[10] SLICE_SELECT_PRE VSS VSS VDD VDD SLICE_SELECT_BUF[10] sky130_fd_sc_hd__buf_2
x12[9] SLICE_SELECT_PRE VSS VSS VDD VDD SLICE_SELECT_BUF[9] sky130_fd_sc_hd__buf_2
x12[8] SLICE_SELECT_PRE VSS VSS VDD VDD SLICE_SELECT_BUF[8] sky130_fd_sc_hd__buf_2
x12[7] SLICE_SELECT_PRE VSS VSS VDD VDD SLICE_SELECT_BUF[7] sky130_fd_sc_hd__buf_2
x12[6] SLICE_SELECT_PRE VSS VSS VDD VDD SLICE_SELECT_BUF[6] sky130_fd_sc_hd__buf_2
x12[5] SLICE_SELECT_PRE VSS VSS VDD VDD SLICE_SELECT_BUF[5] sky130_fd_sc_hd__buf_2
x12[4] SLICE_SELECT_PRE VSS VSS VDD VDD SLICE_SELECT_BUF[4] sky130_fd_sc_hd__buf_2
x12[3] SLICE_SELECT_PRE VSS VSS VDD VDD SLICE_SELECT_BUF[3] sky130_fd_sc_hd__buf_2
x12[2] SLICE_SELECT_PRE VSS VSS VDD VDD SLICE_SELECT_BUF[2] sky130_fd_sc_hd__buf_2
x12[1] SLICE_SELECT_PRE VSS VSS VDD VDD SLICE_SELECT_BUF[1] sky130_fd_sc_hd__buf_2
x12[0] SLICE_SELECT_PRE VSS VSS VDD VDD SLICE_SELECT_BUF[0] sky130_fd_sc_hd__buf_2
* noconn READ_ROUT_BLOCK_SA_EN[15:1],READ_ROUT0_BLOCK_SA_EN
* noconn READ_ROUT_BLOCK_SA_EN_5[15:1],READ_ROUT0_BLOCK_SA_EN_5
* noconn READ_ROUT_BL_EN_5[15:1],READ_ROUT0_BL_EN_5
* noconn READ_ROUT_COL_SELECT0_5[15:1],READ_ROUT0_COL_SELECT0_5
**.ends
.end
